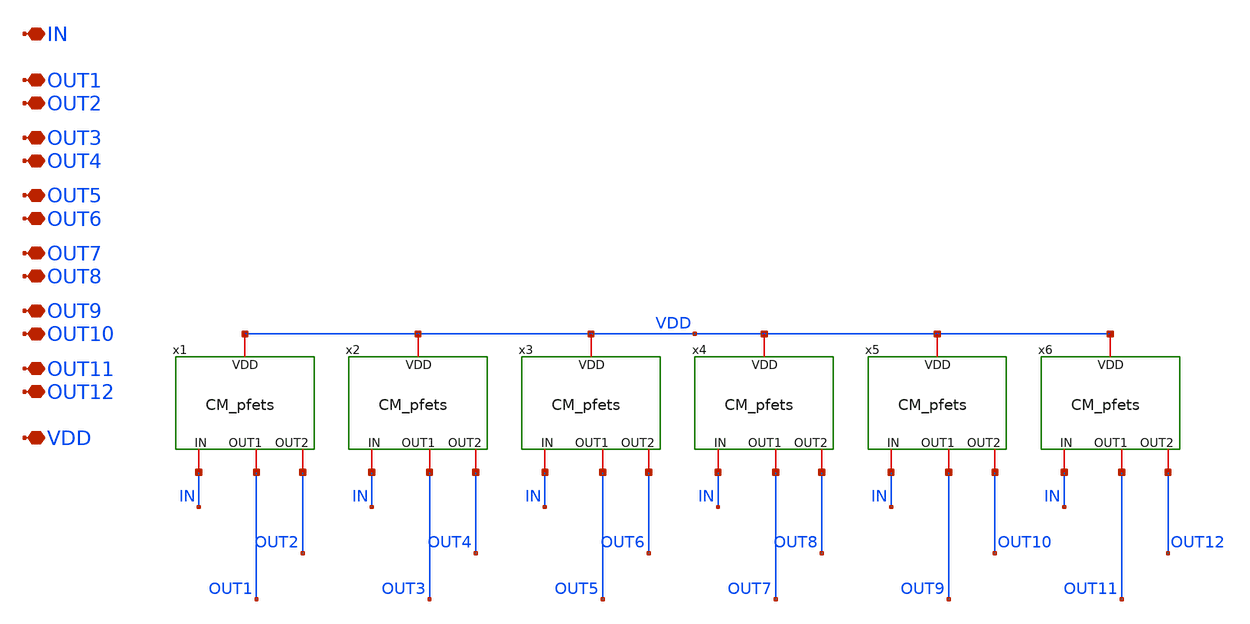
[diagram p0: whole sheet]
** sch_path: TIA_Filter/CurrentMirrors/CM_p_net.sch
**.subckt CM_p_net IN OUT1 OUT2 VDD OUT3 OUT4 OUT5 OUT6 OUT7 OUT8 OUT9 OUT10 OUT11 OUT12
*.iopin IN
*.iopin OUT1
*.iopin OUT2
*.iopin VDD
*.iopin OUT3
*.iopin OUT4
*.iopin OUT5
*.iopin OUT6
*.iopin OUT7
*.iopin OUT8
*.iopin OUT9
*.iopin OUT10
*.iopin OUT11
*.iopin OUT12
x1 IN OUT1 OUT2 VDD CM_pfets
x2 IN OUT3 OUT4 VDD CM_pfets
x3 IN OUT5 OUT6 VDD CM_pfets
x4 IN OUT7 OUT8 VDD CM_pfets
x5 IN OUT9 OUT10 VDD CM_pfets
x6 IN OUT11 OUT12 VDD CM_pfets
**.ends

* expanding   symbol:  CurrentMirrors/CM_pfets.sym # of pins=4
** sym_path: TIA_Filter/CurrentMirrors/CM_pfets.sym
** sch_path: TIA_Filter/CurrentMirrors/CM_pfets.sch
.subckt CM_pfets IN OUT1 OUT2 VDD
*.iopin IN
*.iopin OUT1
*.iopin OUT2
*.iopin VDD
XM1[1] IN IN VDD VDD pfet_03v3 L=2u W=2u nf=1 ad='int((nf+1)/2) * W/nf * 0.18u' as='int((nf+2)/2) * W/nf * 0.18u'
+ pd='2*int((nf+1)/2) * (W/nf + 0.18u)' ps='2*int((nf+2)/2) * (W/nf + 0.18u)' nrd='0.18u / W' nrs='0.18u / W'
+ sa=0 sb=0 sd=0 m=1
XM1[2] IN IN VDD VDD pfet_03v3 L=2u W=2u nf=1 ad='int((nf+1)/2) * W/nf * 0.18u' as='int((nf+2)/2) * W/nf * 0.18u'
+ pd='2*int((nf+1)/2) * (W/nf + 0.18u)' ps='2*int((nf+2)/2) * (W/nf + 0.18u)' nrd='0.18u / W' nrs='0.18u / W'
+ sa=0 sb=0 sd=0 m=1
XM1[3] IN IN VDD VDD pfet_03v3 L=2u W=2u nf=1 ad='int((nf+1)/2) * W/nf * 0.18u' as='int((nf+2)/2) * W/nf * 0.18u'
+ pd='2*int((nf+1)/2) * (W/nf + 0.18u)' ps='2*int((nf+2)/2) * (W/nf + 0.18u)' nrd='0.18u / W' nrs='0.18u / W'
+ sa=0 sb=0 sd=0 m=1
XM1[4] IN IN VDD VDD pfet_03v3 L=2u W=2u nf=1 ad='int((nf+1)/2) * W/nf * 0.18u' as='int((nf+2)/2) * W/nf * 0.18u'
+ pd='2*int((nf+1)/2) * (W/nf + 0.18u)' ps='2*int((nf+2)/2) * (W/nf + 0.18u)' nrd='0.18u / W' nrs='0.18u / W'
+ sa=0 sb=0 sd=0 m=1
XM1[5] IN IN VDD VDD pfet_03v3 L=2u W=2u nf=1 ad='int((nf+1)/2) * W/nf * 0.18u' as='int((nf+2)/2) * W/nf * 0.18u'
+ pd='2*int((nf+1)/2) * (W/nf + 0.18u)' ps='2*int((nf+2)/2) * (W/nf + 0.18u)' nrd='0.18u / W' nrs='0.18u / W'
+ sa=0 sb=0 sd=0 m=1
XM1[6] IN IN VDD VDD pfet_03v3 L=2u W=2u nf=1 ad='int((nf+1)/2) * W/nf * 0.18u' as='int((nf+2)/2) * W/nf * 0.18u'
+ pd='2*int((nf+1)/2) * (W/nf + 0.18u)' ps='2*int((nf+2)/2) * (W/nf + 0.18u)' nrd='0.18u / W' nrs='0.18u / W'
+ sa=0 sb=0 sd=0 m=1
XM2 net4 IN VDD VDD pfet_03v3 L=2u W=2u nf=1 ad='int((nf+1)/2) * W/nf * 0.18u' as='int((nf+2)/2) * W/nf * 0.18u'
+ pd='2*int((nf+1)/2) * (W/nf + 0.18u)' ps='2*int((nf+2)/2) * (W/nf + 0.18u)' nrd='0.18u / W' nrs='0.18u / W'
+ sa=0 sb=0 sd=0 m=1
XM1 net5 IN net4 VDD pfet_03v3 L=2u W=2u nf=1 ad='int((nf+1)/2) * W/nf * 0.18u' as='int((nf+2)/2) * W/nf * 0.18u'
+ pd='2*int((nf+1)/2) * (W/nf + 0.18u)' ps='2*int((nf+2)/2) * (W/nf + 0.18u)' nrd='0.18u / W' nrs='0.18u / W'
+ sa=0 sb=0 sd=0 m=1
XM3 net6 IN net5 VDD pfet_03v3 L=2u W=2u nf=1 ad='int((nf+1)/2) * W/nf * 0.18u' as='int((nf+2)/2) * W/nf * 0.18u'
+ pd='2*int((nf+1)/2) * (W/nf + 0.18u)' ps='2*int((nf+2)/2) * (W/nf + 0.18u)' nrd='0.18u / W' nrs='0.18u / W'
+ sa=0 sb=0 sd=0 m=1
XM4 net7 IN net6 VDD pfet_03v3 L=2u W=2u nf=1 ad='int((nf+1)/2) * W/nf * 0.18u' as='int((nf+2)/2) * W/nf * 0.18u'
+ pd='2*int((nf+1)/2) * (W/nf + 0.18u)' ps='2*int((nf+2)/2) * (W/nf + 0.18u)' nrd='0.18u / W' nrs='0.18u / W'
+ sa=0 sb=0 sd=0 m=1
XM5 net8 IN net7 VDD pfet_03v3 L=2u W=2u nf=1 ad='int((nf+1)/2) * W/nf * 0.18u' as='int((nf+2)/2) * W/nf * 0.18u'
+ pd='2*int((nf+1)/2) * (W/nf + 0.18u)' ps='2*int((nf+2)/2) * (W/nf + 0.18u)' nrd='0.18u / W' nrs='0.18u / W'
+ sa=0 sb=0 sd=0 m=1
XM6 net9 IN net8 VDD pfet_03v3 L=2u W=2u nf=1 ad='int((nf+1)/2) * W/nf * 0.18u' as='int((nf+2)/2) * W/nf * 0.18u'
+ pd='2*int((nf+1)/2) * (W/nf + 0.18u)' ps='2*int((nf+2)/2) * (W/nf + 0.18u)' nrd='0.18u / W' nrs='0.18u / W'
+ sa=0 sb=0 sd=0 m=1
XM7 net10 IN net9 VDD pfet_03v3 L=2u W=2u nf=1 ad='int((nf+1)/2) * W/nf * 0.18u' as='int((nf+2)/2) * W/nf * 0.18u'
+ pd='2*int((nf+1)/2) * (W/nf + 0.18u)' ps='2*int((nf+2)/2) * (W/nf + 0.18u)' nrd='0.18u / W' nrs='0.18u / W'
+ sa=0 sb=0 sd=0 m=1
XM8 net11 IN net10 VDD pfet_03v3 L=2u W=2u nf=1 ad='int((nf+1)/2) * W/nf * 0.18u' as='int((nf+2)/2) * W/nf * 0.18u'
+ pd='2*int((nf+1)/2) * (W/nf + 0.18u)' ps='2*int((nf+2)/2) * (W/nf + 0.18u)' nrd='0.18u / W' nrs='0.18u / W'
+ sa=0 sb=0 sd=0 m=1
XM9 net12 IN net11 VDD pfet_03v3 L=2u W=2u nf=1 ad='int((nf+1)/2) * W/nf * 0.18u' as='int((nf+2)/2) * W/nf * 0.18u'
+ pd='2*int((nf+1)/2) * (W/nf + 0.18u)' ps='2*int((nf+2)/2) * (W/nf + 0.18u)' nrd='0.18u / W' nrs='0.18u / W'
+ sa=0 sb=0 sd=0 m=1
XM10 net1 IN net12 VDD pfet_03v3 L=2u W=2u nf=1 ad='int((nf+1)/2) * W/nf * 0.18u' as='int((nf+2)/2) * W/nf * 0.18u'
+ pd='2*int((nf+1)/2) * (W/nf + 0.18u)' ps='2*int((nf+2)/2) * (W/nf + 0.18u)' nrd='0.18u / W' nrs='0.18u / W'
+ sa=0 sb=0 sd=0 m=1
XM11 net13 IN net1 VDD pfet_03v3 L=2u W=2u nf=1 ad='int((nf+1)/2) * W/nf * 0.18u' as='int((nf+2)/2) * W/nf * 0.18u'
+ pd='2*int((nf+1)/2) * (W/nf + 0.18u)' ps='2*int((nf+2)/2) * (W/nf + 0.18u)' nrd='0.18u / W' nrs='0.18u / W'
+ sa=0 sb=0 sd=0 m=1
XM12 net14 IN net13 VDD pfet_03v3 L=2u W=2u nf=1 ad='int((nf+1)/2) * W/nf * 0.18u' as='int((nf+2)/2) * W/nf * 0.18u'
+ pd='2*int((nf+1)/2) * (W/nf + 0.18u)' ps='2*int((nf+2)/2) * (W/nf + 0.18u)' nrd='0.18u / W' nrs='0.18u / W'
+ sa=0 sb=0 sd=0 m=1
XM13 net15 IN net14 VDD pfet_03v3 L=2u W=2u nf=1 ad='int((nf+1)/2) * W/nf * 0.18u' as='int((nf+2)/2) * W/nf * 0.18u'
+ pd='2*int((nf+1)/2) * (W/nf + 0.18u)' ps='2*int((nf+2)/2) * (W/nf + 0.18u)' nrd='0.18u / W' nrs='0.18u / W'
+ sa=0 sb=0 sd=0 m=1
XM14 net16 IN net15 VDD pfet_03v3 L=2u W=2u nf=1 ad='int((nf+1)/2) * W/nf * 0.18u' as='int((nf+2)/2) * W/nf * 0.18u'
+ pd='2*int((nf+1)/2) * (W/nf + 0.18u)' ps='2*int((nf+2)/2) * (W/nf + 0.18u)' nrd='0.18u / W' nrs='0.18u / W'
+ sa=0 sb=0 sd=0 m=1
XM15 net17 IN net16 VDD pfet_03v3 L=2u W=2u nf=1 ad='int((nf+1)/2) * W/nf * 0.18u' as='int((nf+2)/2) * W/nf * 0.18u'
+ pd='2*int((nf+1)/2) * (W/nf + 0.18u)' ps='2*int((nf+2)/2) * (W/nf + 0.18u)' nrd='0.18u / W' nrs='0.18u / W'
+ sa=0 sb=0 sd=0 m=1
XM16 net18 IN net17 VDD pfet_03v3 L=2u W=2u nf=1 ad='int((nf+1)/2) * W/nf * 0.18u' as='int((nf+2)/2) * W/nf * 0.18u'
+ pd='2*int((nf+1)/2) * (W/nf + 0.18u)' ps='2*int((nf+2)/2) * (W/nf + 0.18u)' nrd='0.18u / W' nrs='0.18u / W'
+ sa=0 sb=0 sd=0 m=1
XM17 net19 IN net18 VDD pfet_03v3 L=2u W=2u nf=1 ad='int((nf+1)/2) * W/nf * 0.18u' as='int((nf+2)/2) * W/nf * 0.18u'
+ pd='2*int((nf+1)/2) * (W/nf + 0.18u)' ps='2*int((nf+2)/2) * (W/nf + 0.18u)' nrd='0.18u / W' nrs='0.18u / W'
+ sa=0 sb=0 sd=0 m=1
XM18 net20 IN net19 VDD pfet_03v3 L=2u W=2u nf=1 ad='int((nf+1)/2) * W/nf * 0.18u' as='int((nf+2)/2) * W/nf * 0.18u'
+ pd='2*int((nf+1)/2) * (W/nf + 0.18u)' ps='2*int((nf+2)/2) * (W/nf + 0.18u)' nrd='0.18u / W' nrs='0.18u / W'
+ sa=0 sb=0 sd=0 m=1
XM19 net21 IN net20 VDD pfet_03v3 L=2u W=2u nf=1 ad='int((nf+1)/2) * W/nf * 0.18u' as='int((nf+2)/2) * W/nf * 0.18u'
+ pd='2*int((nf+1)/2) * (W/nf + 0.18u)' ps='2*int((nf+2)/2) * (W/nf + 0.18u)' nrd='0.18u / W' nrs='0.18u / W'
+ sa=0 sb=0 sd=0 m=1
XM20 net2 IN net21 VDD pfet_03v3 L=2u W=2u nf=1 ad='int((nf+1)/2) * W/nf * 0.18u' as='int((nf+2)/2) * W/nf * 0.18u'
+ pd='2*int((nf+1)/2) * (W/nf + 0.18u)' ps='2*int((nf+2)/2) * (W/nf + 0.18u)' nrd='0.18u / W' nrs='0.18u / W'
+ sa=0 sb=0 sd=0 m=1
XM21 net22 IN net2 VDD pfet_03v3 L=2u W=2u nf=1 ad='int((nf+1)/2) * W/nf * 0.18u' as='int((nf+2)/2) * W/nf * 0.18u'
+ pd='2*int((nf+1)/2) * (W/nf + 0.18u)' ps='2*int((nf+2)/2) * (W/nf + 0.18u)' nrd='0.18u / W' nrs='0.18u / W'
+ sa=0 sb=0 sd=0 m=1
XM22 net23 IN net22 VDD pfet_03v3 L=2u W=2u nf=1 ad='int((nf+1)/2) * W/nf * 0.18u' as='int((nf+2)/2) * W/nf * 0.18u'
+ pd='2*int((nf+1)/2) * (W/nf + 0.18u)' ps='2*int((nf+2)/2) * (W/nf + 0.18u)' nrd='0.18u / W' nrs='0.18u / W'
+ sa=0 sb=0 sd=0 m=1
XM23 net24 IN net23 VDD pfet_03v3 L=2u W=2u nf=1 ad='int((nf+1)/2) * W/nf * 0.18u' as='int((nf+2)/2) * W/nf * 0.18u'
+ pd='2*int((nf+1)/2) * (W/nf + 0.18u)' ps='2*int((nf+2)/2) * (W/nf + 0.18u)' nrd='0.18u / W' nrs='0.18u / W'
+ sa=0 sb=0 sd=0 m=1
XM24 net25 IN net24 VDD pfet_03v3 L=2u W=2u nf=1 ad='int((nf+1)/2) * W/nf * 0.18u' as='int((nf+2)/2) * W/nf * 0.18u'
+ pd='2*int((nf+1)/2) * (W/nf + 0.18u)' ps='2*int((nf+2)/2) * (W/nf + 0.18u)' nrd='0.18u / W' nrs='0.18u / W'
+ sa=0 sb=0 sd=0 m=1
XM25 net26 IN net25 VDD pfet_03v3 L=2u W=2u nf=1 ad='int((nf+1)/2) * W/nf * 0.18u' as='int((nf+2)/2) * W/nf * 0.18u'
+ pd='2*int((nf+1)/2) * (W/nf + 0.18u)' ps='2*int((nf+2)/2) * (W/nf + 0.18u)' nrd='0.18u / W' nrs='0.18u / W'
+ sa=0 sb=0 sd=0 m=1
XM26 net27 IN net26 VDD pfet_03v3 L=2u W=2u nf=1 ad='int((nf+1)/2) * W/nf * 0.18u' as='int((nf+2)/2) * W/nf * 0.18u'
+ pd='2*int((nf+1)/2) * (W/nf + 0.18u)' ps='2*int((nf+2)/2) * (W/nf + 0.18u)' nrd='0.18u / W' nrs='0.18u / W'
+ sa=0 sb=0 sd=0 m=1
XM27 net28 IN net27 VDD pfet_03v3 L=2u W=2u nf=1 ad='int((nf+1)/2) * W/nf * 0.18u' as='int((nf+2)/2) * W/nf * 0.18u'
+ pd='2*int((nf+1)/2) * (W/nf + 0.18u)' ps='2*int((nf+2)/2) * (W/nf + 0.18u)' nrd='0.18u / W' nrs='0.18u / W'
+ sa=0 sb=0 sd=0 m=1
XM28 net29 IN net28 VDD pfet_03v3 L=2u W=2u nf=1 ad='int((nf+1)/2) * W/nf * 0.18u' as='int((nf+2)/2) * W/nf * 0.18u'
+ pd='2*int((nf+1)/2) * (W/nf + 0.18u)' ps='2*int((nf+2)/2) * (W/nf + 0.18u)' nrd='0.18u / W' nrs='0.18u / W'
+ sa=0 sb=0 sd=0 m=1
XM29 net30 IN net29 VDD pfet_03v3 L=2u W=2u nf=1 ad='int((nf+1)/2) * W/nf * 0.18u' as='int((nf+2)/2) * W/nf * 0.18u'
+ pd='2*int((nf+1)/2) * (W/nf + 0.18u)' ps='2*int((nf+2)/2) * (W/nf + 0.18u)' nrd='0.18u / W' nrs='0.18u / W'
+ sa=0 sb=0 sd=0 m=1
XM30 OUT1 IN net30 VDD pfet_03v3 L=2u W=2u nf=1 ad='int((nf+1)/2) * W/nf * 0.18u' as='int((nf+2)/2) * W/nf * 0.18u'
+ pd='2*int((nf+1)/2) * (W/nf + 0.18u)' ps='2*int((nf+2)/2) * (W/nf + 0.18u)' nrd='0.18u / W' nrs='0.18u / W'
+ sa=0 sb=0 sd=0 m=1
XM31 net31 IN VDD VDD pfet_03v3 L=2u W=2u nf=1 ad='int((nf+1)/2) * W/nf * 0.18u' as='int((nf+2)/2) * W/nf * 0.18u'
+ pd='2*int((nf+1)/2) * (W/nf + 0.18u)' ps='2*int((nf+2)/2) * (W/nf + 0.18u)' nrd='0.18u / W' nrs='0.18u / W'
+ sa=0 sb=0 sd=0 m=1
XM32 net32 IN net31 VDD pfet_03v3 L=2u W=2u nf=1 ad='int((nf+1)/2) * W/nf * 0.18u' as='int((nf+2)/2) * W/nf * 0.18u'
+ pd='2*int((nf+1)/2) * (W/nf + 0.18u)' ps='2*int((nf+2)/2) * (W/nf + 0.18u)' nrd='0.18u / W' nrs='0.18u / W'
+ sa=0 sb=0 sd=0 m=1
XM33 net33 IN net32 VDD pfet_03v3 L=2u W=2u nf=1 ad='int((nf+1)/2) * W/nf * 0.18u' as='int((nf+2)/2) * W/nf * 0.18u'
+ pd='2*int((nf+1)/2) * (W/nf + 0.18u)' ps='2*int((nf+2)/2) * (W/nf + 0.18u)' nrd='0.18u / W' nrs='0.18u / W'
+ sa=0 sb=0 sd=0 m=1
XM34 net34 IN net33 VDD pfet_03v3 L=2u W=2u nf=1 ad='int((nf+1)/2) * W/nf * 0.18u' as='int((nf+2)/2) * W/nf * 0.18u'
+ pd='2*int((nf+1)/2) * (W/nf + 0.18u)' ps='2*int((nf+2)/2) * (W/nf + 0.18u)' nrd='0.18u / W' nrs='0.18u / W'
+ sa=0 sb=0 sd=0 m=1
XM35 net35 IN net34 VDD pfet_03v3 L=2u W=2u nf=1 ad='int((nf+1)/2) * W/nf * 0.18u' as='int((nf+2)/2) * W/nf * 0.18u'
+ pd='2*int((nf+1)/2) * (W/nf + 0.18u)' ps='2*int((nf+2)/2) * (W/nf + 0.18u)' nrd='0.18u / W' nrs='0.18u / W'
+ sa=0 sb=0 sd=0 m=1
XM36 net36 IN net35 VDD pfet_03v3 L=2u W=2u nf=1 ad='int((nf+1)/2) * W/nf * 0.18u' as='int((nf+2)/2) * W/nf * 0.18u'
+ pd='2*int((nf+1)/2) * (W/nf + 0.18u)' ps='2*int((nf+2)/2) * (W/nf + 0.18u)' nrd='0.18u / W' nrs='0.18u / W'
+ sa=0 sb=0 sd=0 m=1
XM37 net37 IN net36 VDD pfet_03v3 L=2u W=2u nf=1 ad='int((nf+1)/2) * W/nf * 0.18u' as='int((nf+2)/2) * W/nf * 0.18u'
+ pd='2*int((nf+1)/2) * (W/nf + 0.18u)' ps='2*int((nf+2)/2) * (W/nf + 0.18u)' nrd='0.18u / W' nrs='0.18u / W'
+ sa=0 sb=0 sd=0 m=1
XM38 net38 IN net37 VDD pfet_03v3 L=2u W=2u nf=1 ad='int((nf+1)/2) * W/nf * 0.18u' as='int((nf+2)/2) * W/nf * 0.18u'
+ pd='2*int((nf+1)/2) * (W/nf + 0.18u)' ps='2*int((nf+2)/2) * (W/nf + 0.18u)' nrd='0.18u / W' nrs='0.18u / W'
+ sa=0 sb=0 sd=0 m=1
XM39 net39 IN net38 VDD pfet_03v3 L=2u W=2u nf=1 ad='int((nf+1)/2) * W/nf * 0.18u' as='int((nf+2)/2) * W/nf * 0.18u'
+ pd='2*int((nf+1)/2) * (W/nf + 0.18u)' ps='2*int((nf+2)/2) * (W/nf + 0.18u)' nrd='0.18u / W' nrs='0.18u / W'
+ sa=0 sb=0 sd=0 m=1
XM40 net3 IN net39 VDD pfet_03v3 L=2u W=2u nf=1 ad='int((nf+1)/2) * W/nf * 0.18u' as='int((nf+2)/2) * W/nf * 0.18u'
+ pd='2*int((nf+1)/2) * (W/nf + 0.18u)' ps='2*int((nf+2)/2) * (W/nf + 0.18u)' nrd='0.18u / W' nrs='0.18u / W'
+ sa=0 sb=0 sd=0 m=1
XM41 net40 IN net3 VDD pfet_03v3 L=2u W=2u nf=1 ad='int((nf+1)/2) * W/nf * 0.18u' as='int((nf+2)/2) * W/nf * 0.18u'
+ pd='2*int((nf+1)/2) * (W/nf + 0.18u)' ps='2*int((nf+2)/2) * (W/nf + 0.18u)' nrd='0.18u / W' nrs='0.18u / W'
+ sa=0 sb=0 sd=0 m=1
XM42 net41 IN net40 VDD pfet_03v3 L=2u W=2u nf=1 ad='int((nf+1)/2) * W/nf * 0.18u' as='int((nf+2)/2) * W/nf * 0.18u'
+ pd='2*int((nf+1)/2) * (W/nf + 0.18u)' ps='2*int((nf+2)/2) * (W/nf + 0.18u)' nrd='0.18u / W' nrs='0.18u / W'
+ sa=0 sb=0 sd=0 m=1
XM43 net42 IN net41 VDD pfet_03v3 L=2u W=2u nf=1 ad='int((nf+1)/2) * W/nf * 0.18u' as='int((nf+2)/2) * W/nf * 0.18u'
+ pd='2*int((nf+1)/2) * (W/nf + 0.18u)' ps='2*int((nf+2)/2) * (W/nf + 0.18u)' nrd='0.18u / W' nrs='0.18u / W'
+ sa=0 sb=0 sd=0 m=1
XM44 OUT2 IN net42 VDD pfet_03v3 L=2u W=2u nf=1 ad='int((nf+1)/2) * W/nf * 0.18u' as='int((nf+2)/2) * W/nf * 0.18u'
+ pd='2*int((nf+1)/2) * (W/nf + 0.18u)' ps='2*int((nf+2)/2) * (W/nf + 0.18u)' nrd='0.18u / W' nrs='0.18u / W'
+ sa=0 sb=0 sd=0 m=1
XM2[1] VDD VDD VDD VDD pfet_03v3 L=2u W=2u nf=1 ad='int((nf+1)/2) * W/nf * 0.18u' as='int((nf+2)/2) * W/nf * 0.18u'
+ pd='2*int((nf+1)/2) * (W/nf + 0.18u)' ps='2*int((nf+2)/2) * (W/nf + 0.18u)' nrd='0.18u / W' nrs='0.18u / W'
+ sa=0 sb=0 sd=0 m=1
XM2[2] VDD VDD VDD VDD pfet_03v3 L=2u W=2u nf=1 ad='int((nf+1)/2) * W/nf * 0.18u' as='int((nf+2)/2) * W/nf * 0.18u'
+ pd='2*int((nf+1)/2) * (W/nf + 0.18u)' ps='2*int((nf+2)/2) * (W/nf + 0.18u)' nrd='0.18u / W' nrs='0.18u / W'
+ sa=0 sb=0 sd=0 m=1
XM2[3] VDD VDD VDD VDD pfet_03v3 L=2u W=2u nf=1 ad='int((nf+1)/2) * W/nf * 0.18u' as='int((nf+2)/2) * W/nf * 0.18u'
+ pd='2*int((nf+1)/2) * (W/nf + 0.18u)' ps='2*int((nf+2)/2) * (W/nf + 0.18u)' nrd='0.18u / W' nrs='0.18u / W'
+ sa=0 sb=0 sd=0 m=1
XM2[4] VDD VDD VDD VDD pfet_03v3 L=2u W=2u nf=1 ad='int((nf+1)/2) * W/nf * 0.18u' as='int((nf+2)/2) * W/nf * 0.18u'
+ pd='2*int((nf+1)/2) * (W/nf + 0.18u)' ps='2*int((nf+2)/2) * (W/nf + 0.18u)' nrd='0.18u / W' nrs='0.18u / W'
+ sa=0 sb=0 sd=0 m=1
XM2[5] VDD VDD VDD VDD pfet_03v3 L=2u W=2u nf=1 ad='int((nf+1)/2) * W/nf * 0.18u' as='int((nf+2)/2) * W/nf * 0.18u'
+ pd='2*int((nf+1)/2) * (W/nf + 0.18u)' ps='2*int((nf+2)/2) * (W/nf + 0.18u)' nrd='0.18u / W' nrs='0.18u / W'
+ sa=0 sb=0 sd=0 m=1
XM2[6] VDD VDD VDD VDD pfet_03v3 L=2u W=2u nf=1 ad='int((nf+1)/2) * W/nf * 0.18u' as='int((nf+2)/2) * W/nf * 0.18u'
+ pd='2*int((nf+1)/2) * (W/nf + 0.18u)' ps='2*int((nf+2)/2) * (W/nf + 0.18u)' nrd='0.18u / W' nrs='0.18u / W'
+ sa=0 sb=0 sd=0 m=1
XM2[7] VDD VDD VDD VDD pfet_03v3 L=2u W=2u nf=1 ad='int((nf+1)/2) * W/nf * 0.18u' as='int((nf+2)/2) * W/nf * 0.18u'
+ pd='2*int((nf+1)/2) * (W/nf + 0.18u)' ps='2*int((nf+2)/2) * (W/nf + 0.18u)' nrd='0.18u / W' nrs='0.18u / W'
+ sa=0 sb=0 sd=0 m=1
XM2[8] VDD VDD VDD VDD pfet_03v3 L=2u W=2u nf=1 ad='int((nf+1)/2) * W/nf * 0.18u' as='int((nf+2)/2) * W/nf * 0.18u'
+ pd='2*int((nf+1)/2) * (W/nf + 0.18u)' ps='2*int((nf+2)/2) * (W/nf + 0.18u)' nrd='0.18u / W' nrs='0.18u / W'
+ sa=0 sb=0 sd=0 m=1
XM2[9] VDD VDD VDD VDD pfet_03v3 L=2u W=2u nf=1 ad='int((nf+1)/2) * W/nf * 0.18u' as='int((nf+2)/2) * W/nf * 0.18u'
+ pd='2*int((nf+1)/2) * (W/nf + 0.18u)' ps='2*int((nf+2)/2) * (W/nf + 0.18u)' nrd='0.18u / W' nrs='0.18u / W'
+ sa=0 sb=0 sd=0 m=1
XM2[10] VDD VDD VDD VDD pfet_03v3 L=2u W=2u nf=1 ad='int((nf+1)/2) * W/nf * 0.18u' as='int((nf+2)/2) * W/nf * 0.18u'
+ pd='2*int((nf+1)/2) * (W/nf + 0.18u)' ps='2*int((nf+2)/2) * (W/nf + 0.18u)' nrd='0.18u / W' nrs='0.18u / W'
+ sa=0 sb=0 sd=0 m=1
XM2[11] VDD VDD VDD VDD pfet_03v3 L=2u W=2u nf=1 ad='int((nf+1)/2) * W/nf * 0.18u' as='int((nf+2)/2) * W/nf * 0.18u'
+ pd='2*int((nf+1)/2) * (W/nf + 0.18u)' ps='2*int((nf+2)/2) * (W/nf + 0.18u)' nrd='0.18u / W' nrs='0.18u / W'
+ sa=0 sb=0 sd=0 m=1
XM2[12] VDD VDD VDD VDD pfet_03v3 L=2u W=2u nf=1 ad='int((nf+1)/2) * W/nf * 0.18u' as='int((nf+2)/2) * W/nf * 0.18u'
+ pd='2*int((nf+1)/2) * (W/nf + 0.18u)' ps='2*int((nf+2)/2) * (W/nf + 0.18u)' nrd='0.18u / W' nrs='0.18u / W'
+ sa=0 sb=0 sd=0 m=1
XM2[13] VDD VDD VDD VDD pfet_03v3 L=2u W=2u nf=1 ad='int((nf+1)/2) * W/nf * 0.18u' as='int((nf+2)/2) * W/nf * 0.18u'
+ pd='2*int((nf+1)/2) * (W/nf + 0.18u)' ps='2*int((nf+2)/2) * (W/nf + 0.18u)' nrd='0.18u / W' nrs='0.18u / W'
+ sa=0 sb=0 sd=0 m=1
XM2[14] VDD VDD VDD VDD pfet_03v3 L=2u W=2u nf=1 ad='int((nf+1)/2) * W/nf * 0.18u' as='int((nf+2)/2) * W/nf * 0.18u'
+ pd='2*int((nf+1)/2) * (W/nf + 0.18u)' ps='2*int((nf+2)/2) * (W/nf + 0.18u)' nrd='0.18u / W' nrs='0.18u / W'
+ sa=0 sb=0 sd=0 m=1
XM2[15] VDD VDD VDD VDD pfet_03v3 L=2u W=2u nf=1 ad='int((nf+1)/2) * W/nf * 0.18u' as='int((nf+2)/2) * W/nf * 0.18u'
+ pd='2*int((nf+1)/2) * (W/nf + 0.18u)' ps='2*int((nf+2)/2) * (W/nf + 0.18u)' nrd='0.18u / W' nrs='0.18u / W'
+ sa=0 sb=0 sd=0 m=1
XM2[16] VDD VDD VDD VDD pfet_03v3 L=2u W=2u nf=1 ad='int((nf+1)/2) * W/nf * 0.18u' as='int((nf+2)/2) * W/nf * 0.18u'
+ pd='2*int((nf+1)/2) * (W/nf + 0.18u)' ps='2*int((nf+2)/2) * (W/nf + 0.18u)' nrd='0.18u / W' nrs='0.18u / W'
+ sa=0 sb=0 sd=0 m=1
XM2[17] VDD VDD VDD VDD pfet_03v3 L=2u W=2u nf=1 ad='int((nf+1)/2) * W/nf * 0.18u' as='int((nf+2)/2) * W/nf * 0.18u'
+ pd='2*int((nf+1)/2) * (W/nf + 0.18u)' ps='2*int((nf+2)/2) * (W/nf + 0.18u)' nrd='0.18u / W' nrs='0.18u / W'
+ sa=0 sb=0 sd=0 m=1
XM2[18] VDD VDD VDD VDD pfet_03v3 L=2u W=2u nf=1 ad='int((nf+1)/2) * W/nf * 0.18u' as='int((nf+2)/2) * W/nf * 0.18u'
+ pd='2*int((nf+1)/2) * (W/nf + 0.18u)' ps='2*int((nf+2)/2) * (W/nf + 0.18u)' nrd='0.18u / W' nrs='0.18u / W'
+ sa=0 sb=0 sd=0 m=1
XM2[19] VDD VDD VDD VDD pfet_03v3 L=2u W=2u nf=1 ad='int((nf+1)/2) * W/nf * 0.18u' as='int((nf+2)/2) * W/nf * 0.18u'
+ pd='2*int((nf+1)/2) * (W/nf + 0.18u)' ps='2*int((nf+2)/2) * (W/nf + 0.18u)' nrd='0.18u / W' nrs='0.18u / W'
+ sa=0 sb=0 sd=0 m=1
XM2[20] VDD VDD VDD VDD pfet_03v3 L=2u W=2u nf=1 ad='int((nf+1)/2) * W/nf * 0.18u' as='int((nf+2)/2) * W/nf * 0.18u'
+ pd='2*int((nf+1)/2) * (W/nf + 0.18u)' ps='2*int((nf+2)/2) * (W/nf + 0.18u)' nrd='0.18u / W' nrs='0.18u / W'
+ sa=0 sb=0 sd=0 m=1
XM2[21] VDD VDD VDD VDD pfet_03v3 L=2u W=2u nf=1 ad='int((nf+1)/2) * W/nf * 0.18u' as='int((nf+2)/2) * W/nf * 0.18u'
+ pd='2*int((nf+1)/2) * (W/nf + 0.18u)' ps='2*int((nf+2)/2) * (W/nf + 0.18u)' nrd='0.18u / W' nrs='0.18u / W'
+ sa=0 sb=0 sd=0 m=1
XM2[22] VDD VDD VDD VDD pfet_03v3 L=2u W=2u nf=1 ad='int((nf+1)/2) * W/nf * 0.18u' as='int((nf+2)/2) * W/nf * 0.18u'
+ pd='2*int((nf+1)/2) * (W/nf + 0.18u)' ps='2*int((nf+2)/2) * (W/nf + 0.18u)' nrd='0.18u / W' nrs='0.18u / W'
+ sa=0 sb=0 sd=0 m=1
XM2[23] VDD VDD VDD VDD pfet_03v3 L=2u W=2u nf=1 ad='int((nf+1)/2) * W/nf * 0.18u' as='int((nf+2)/2) * W/nf * 0.18u'
+ pd='2*int((nf+1)/2) * (W/nf + 0.18u)' ps='2*int((nf+2)/2) * (W/nf + 0.18u)' nrd='0.18u / W' nrs='0.18u / W'
+ sa=0 sb=0 sd=0 m=1
XM2[24] VDD VDD VDD VDD pfet_03v3 L=2u W=2u nf=1 ad='int((nf+1)/2) * W/nf * 0.18u' as='int((nf+2)/2) * W/nf * 0.18u'
+ pd='2*int((nf+1)/2) * (W/nf + 0.18u)' ps='2*int((nf+2)/2) * (W/nf + 0.18u)' nrd='0.18u / W' nrs='0.18u / W'
+ sa=0 sb=0 sd=0 m=1
XM2[25] VDD VDD VDD VDD pfet_03v3 L=2u W=2u nf=1 ad='int((nf+1)/2) * W/nf * 0.18u' as='int((nf+2)/2) * W/nf * 0.18u'
+ pd='2*int((nf+1)/2) * (W/nf + 0.18u)' ps='2*int((nf+2)/2) * (W/nf + 0.18u)' nrd='0.18u / W' nrs='0.18u / W'
+ sa=0 sb=0 sd=0 m=1
XM2[26] VDD VDD VDD VDD pfet_03v3 L=2u W=2u nf=1 ad='int((nf+1)/2) * W/nf * 0.18u' as='int((nf+2)/2) * W/nf * 0.18u'
+ pd='2*int((nf+1)/2) * (W/nf + 0.18u)' ps='2*int((nf+2)/2) * (W/nf + 0.18u)' nrd='0.18u / W' nrs='0.18u / W'
+ sa=0 sb=0 sd=0 m=1
XM2[27] VDD VDD VDD VDD pfet_03v3 L=2u W=2u nf=1 ad='int((nf+1)/2) * W/nf * 0.18u' as='int((nf+2)/2) * W/nf * 0.18u'
+ pd='2*int((nf+1)/2) * (W/nf + 0.18u)' ps='2*int((nf+2)/2) * (W/nf + 0.18u)' nrd='0.18u / W' nrs='0.18u / W'
+ sa=0 sb=0 sd=0 m=1
XM2[28] VDD VDD VDD VDD pfet_03v3 L=2u W=2u nf=1 ad='int((nf+1)/2) * W/nf * 0.18u' as='int((nf+2)/2) * W/nf * 0.18u'
+ pd='2*int((nf+1)/2) * (W/nf + 0.18u)' ps='2*int((nf+2)/2) * (W/nf + 0.18u)' nrd='0.18u / W' nrs='0.18u / W'
+ sa=0 sb=0 sd=0 m=1
XM2[29] VDD VDD VDD VDD pfet_03v3 L=2u W=2u nf=1 ad='int((nf+1)/2) * W/nf * 0.18u' as='int((nf+2)/2) * W/nf * 0.18u'
+ pd='2*int((nf+1)/2) * (W/nf + 0.18u)' ps='2*int((nf+2)/2) * (W/nf + 0.18u)' nrd='0.18u / W' nrs='0.18u / W'
+ sa=0 sb=0 sd=0 m=1
XM2[30] VDD VDD VDD VDD pfet_03v3 L=2u W=2u nf=1 ad='int((nf+1)/2) * W/nf * 0.18u' as='int((nf+2)/2) * W/nf * 0.18u'
+ pd='2*int((nf+1)/2) * (W/nf + 0.18u)' ps='2*int((nf+2)/2) * (W/nf + 0.18u)' nrd='0.18u / W' nrs='0.18u / W'
+ sa=0 sb=0 sd=0 m=1
XM2[31] VDD VDD VDD VDD pfet_03v3 L=2u W=2u nf=1 ad='int((nf+1)/2) * W/nf * 0.18u' as='int((nf+2)/2) * W/nf * 0.18u'
+ pd='2*int((nf+1)/2) * (W/nf + 0.18u)' ps='2*int((nf+2)/2) * (W/nf + 0.18u)' nrd='0.18u / W' nrs='0.18u / W'
+ sa=0 sb=0 sd=0 m=1
XM2[32] VDD VDD VDD VDD pfet_03v3 L=2u W=2u nf=1 ad='int((nf+1)/2) * W/nf * 0.18u' as='int((nf+2)/2) * W/nf * 0.18u'
+ pd='2*int((nf+1)/2) * (W/nf + 0.18u)' ps='2*int((nf+2)/2) * (W/nf + 0.18u)' nrd='0.18u / W' nrs='0.18u / W'
+ sa=0 sb=0 sd=0 m=1
XM2[33] VDD VDD VDD VDD pfet_03v3 L=2u W=2u nf=1 ad='int((nf+1)/2) * W/nf * 0.18u' as='int((nf+2)/2) * W/nf * 0.18u'
+ pd='2*int((nf+1)/2) * (W/nf + 0.18u)' ps='2*int((nf+2)/2) * (W/nf + 0.18u)' nrd='0.18u / W' nrs='0.18u / W'
+ sa=0 sb=0 sd=0 m=1
XM2[34] VDD VDD VDD VDD pfet_03v3 L=2u W=2u nf=1 ad='int((nf+1)/2) * W/nf * 0.18u' as='int((nf+2)/2) * W/nf * 0.18u'
+ pd='2*int((nf+1)/2) * (W/nf + 0.18u)' ps='2*int((nf+2)/2) * (W/nf + 0.18u)' nrd='0.18u / W' nrs='0.18u / W'
+ sa=0 sb=0 sd=0 m=1
.ends

.end
